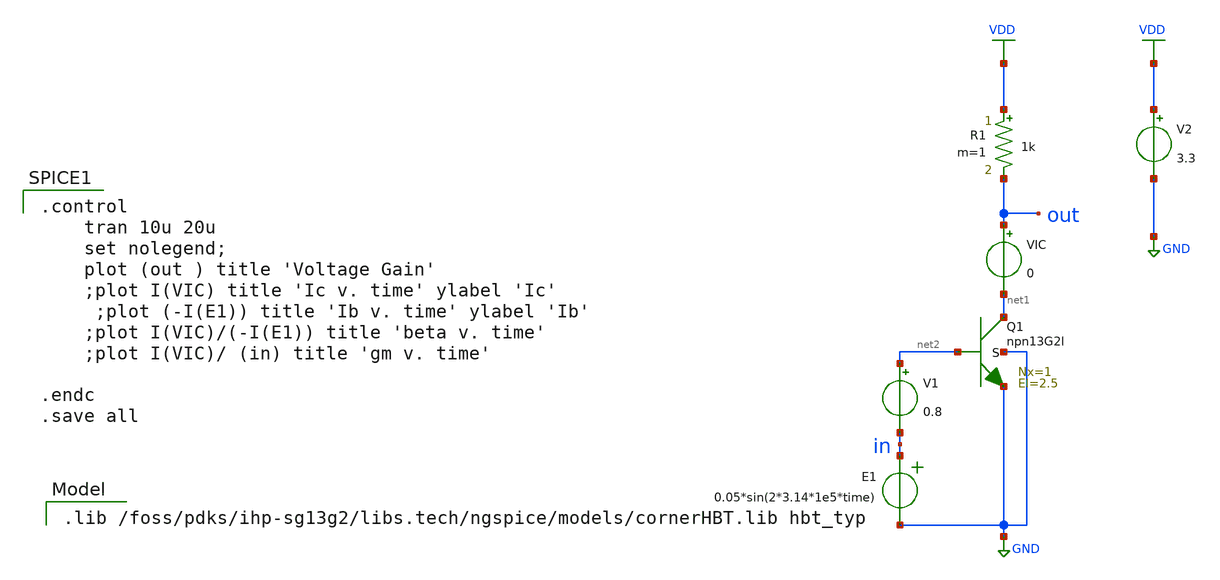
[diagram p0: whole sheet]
** sch_path: sim_backup/simulations/simple_CE_amp.sch
**.subckt simple_CE_amp
XQ1 net1 net2 GND GND npn13G2l Nx=1 El=2.5 mm_ok=1
V1 net2 in 0.8
E1 in GND VOL=' 0.05*sin(2*3.14*1e5*time) '
R1 VDD out 1k m=1
V2 VDD GND 3.3
VIC out net1 0
**** begin user architecture code

.lib /foss/pdks/ihp-sg13g2/libs.tech/ngspice/models/cornerHBT.lib hbt_typ


.control
	tran 10u 20u
	set nolegend;
	plot (out ) title 'Voltage Gain'
	;plot I(VIC) title 'Ic v. time' ylabel 'Ic'
 	;plot (-I(E1)) title 'Ib v. time' ylabel 'Ib'
	;plot I(VIC)/(-I(E1)) title 'beta v. time'
	;plot I(VIC)/ (in) title 'gm v. time'

.endc
.save all

**** end user architecture code
**.ends
.GLOBAL VDD
.GLOBAL GND
.end
